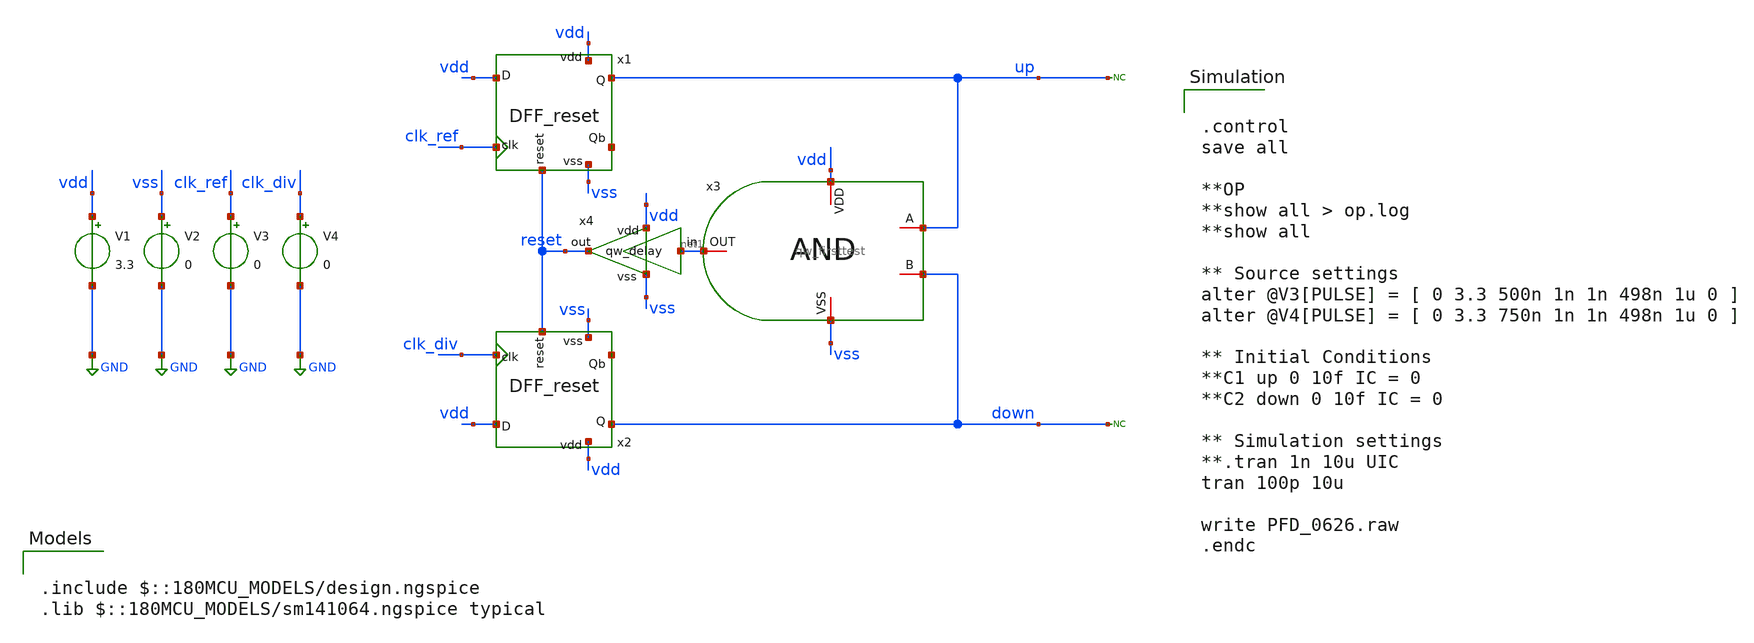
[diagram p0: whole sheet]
** sch_path: designs/libs/core_analog/new_PFD/PFD_0626.sch
**.subckt PFD_0626
x3 vdd net1 up down vss qw_firsttest
x1 vdd up vdd vss reset net2 clk_ref DFF_reset
x2 vdd down vdd vss reset net3 clk_div DFF_reset
V1 vdd GND 3.3
V2 vss GND 0
V3 clk_ref GND 0
V4 clk_div GND 0
* noconn up
* noconn down
x4 vdd net1 reset vss qw_DELAY
**** begin user architecture code

.include $::180MCU_MODELS/design.ngspice
.lib $::180MCU_MODELS/sm141064.ngspice typical



.control
save all

**OP
**show all > op.log
**show all

** Source settings
alter @V3[PULSE] = [ 0 3.3 500n 1n 1n 498n 1u 0 ]
alter @V4[PULSE] = [ 0 3.3 750n 1n 1n 498n 1u 0 ]

** Initial Conditions
**C1 up 0 10f IC = 0
**C2 down 0 10f IC = 0

** Simulation settings
**.tran 1n 10u UIC
tran 100p 10u

write PFD_0626.raw
.endc


**** end user architecture code
**.ends
.GLOBAL GND
.end
